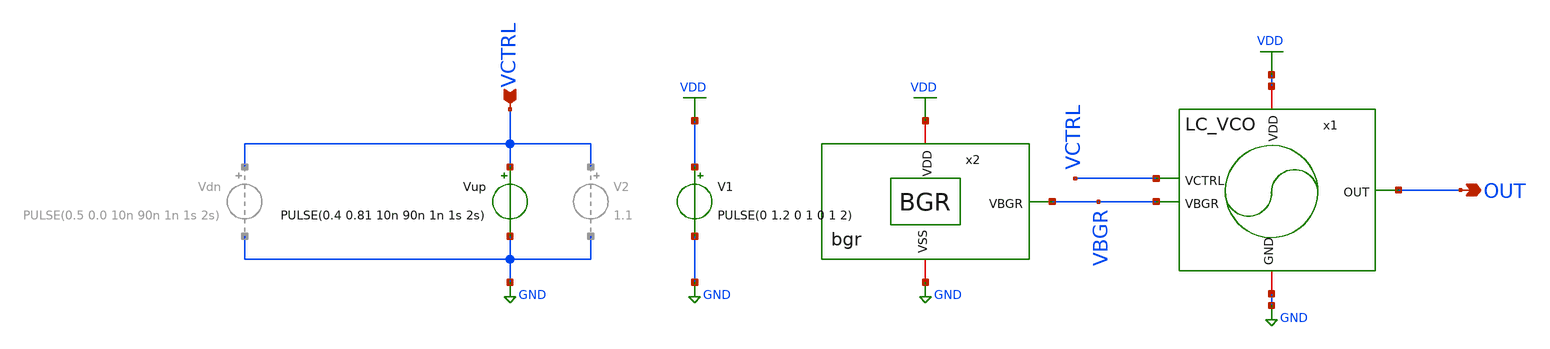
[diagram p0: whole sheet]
** sch_path: schematic/lc-vco/LC_VCO_tb.sch
**.subckt LC_VCO_tb OUT VCTRL
*.opin OUT
*.ipin VCTRL
Vup VCTRL GND PULSE(0.4 0.81 10n 90n 1n 1s 2s)
x1 VDD VCTRL GND OUT VBGR LC_VCO
x2 VBGR VDD GND bgr
V1 VDD GND PULSE(0 1.2 0 1 0 1 2)
**** begin user architecture code



.param temp = 27
.options method=gear, rshunt=1.0e12

.control

* Save required signals
save v(VCTRL) v(OUT) v(x1.Vx) v(vbgr)

* Long transient simulation
tran 10p 1.5 100n

* Save raw waveform
write LC_VCO_tran.raw

* Plot transient waveform
let vout = v(OUT)
plot v(VCTRL) v(x1.Vx) v(OUT)
plot v(VBGR)
* Plot steady-state waveform
plot v(VCTRL) v(x1.Vx) v(OUT) xlimit 1 1100m

* FFT analysis
setplot tran1
linearize vout
set specwindow=blackman
fft vout

* Plot FFT spectrum
let power_out_db = db(vout)
plot power_out_db xlimit 2.38G 2.58G ylimit -200 0

* Find the maximum magnitude value between 2G and 3G
meas sp max_power_out_db max power_out_db FROM=2G TO=3G

* Save FFT spectrum as raw file
write LC_VCO_fft.raw

* Save FFT data
wrdata fft_output_standalone.txt frequency power_out_db

* Save waveform for external processing
wrdata vco_waveform_standalone.txt power_out_db

.endc






.include LC_VCO_standalone_tb.save
.param temp=27
.control
save all
op
write LC_VCO_standalone_tb.raw
.endc






.param L_CC=0.13u

  .param W_34=34.52u
  .param n_34=10

  .param W_12=25.11u
  .param n_12=8

.param L_TL=0.5u

  .param W_5=70.29u
  .param n_5=20

  .param W_6=17.95u
  .param n_6=6

  .param W_7=16.72u
  .param n_7=6




.include ../ihp_4nh_inductor.spice


.lib cornerMOSlv.lib mos_tt
.lib cornerMOShv.lib mos_tt
.lib cornerRES.lib res_typ
.lib cornerCAP.lib cap_typ

**** end user architecture code
**.ends
.GLOBAL GND
.GLOBAL VDD
.end
